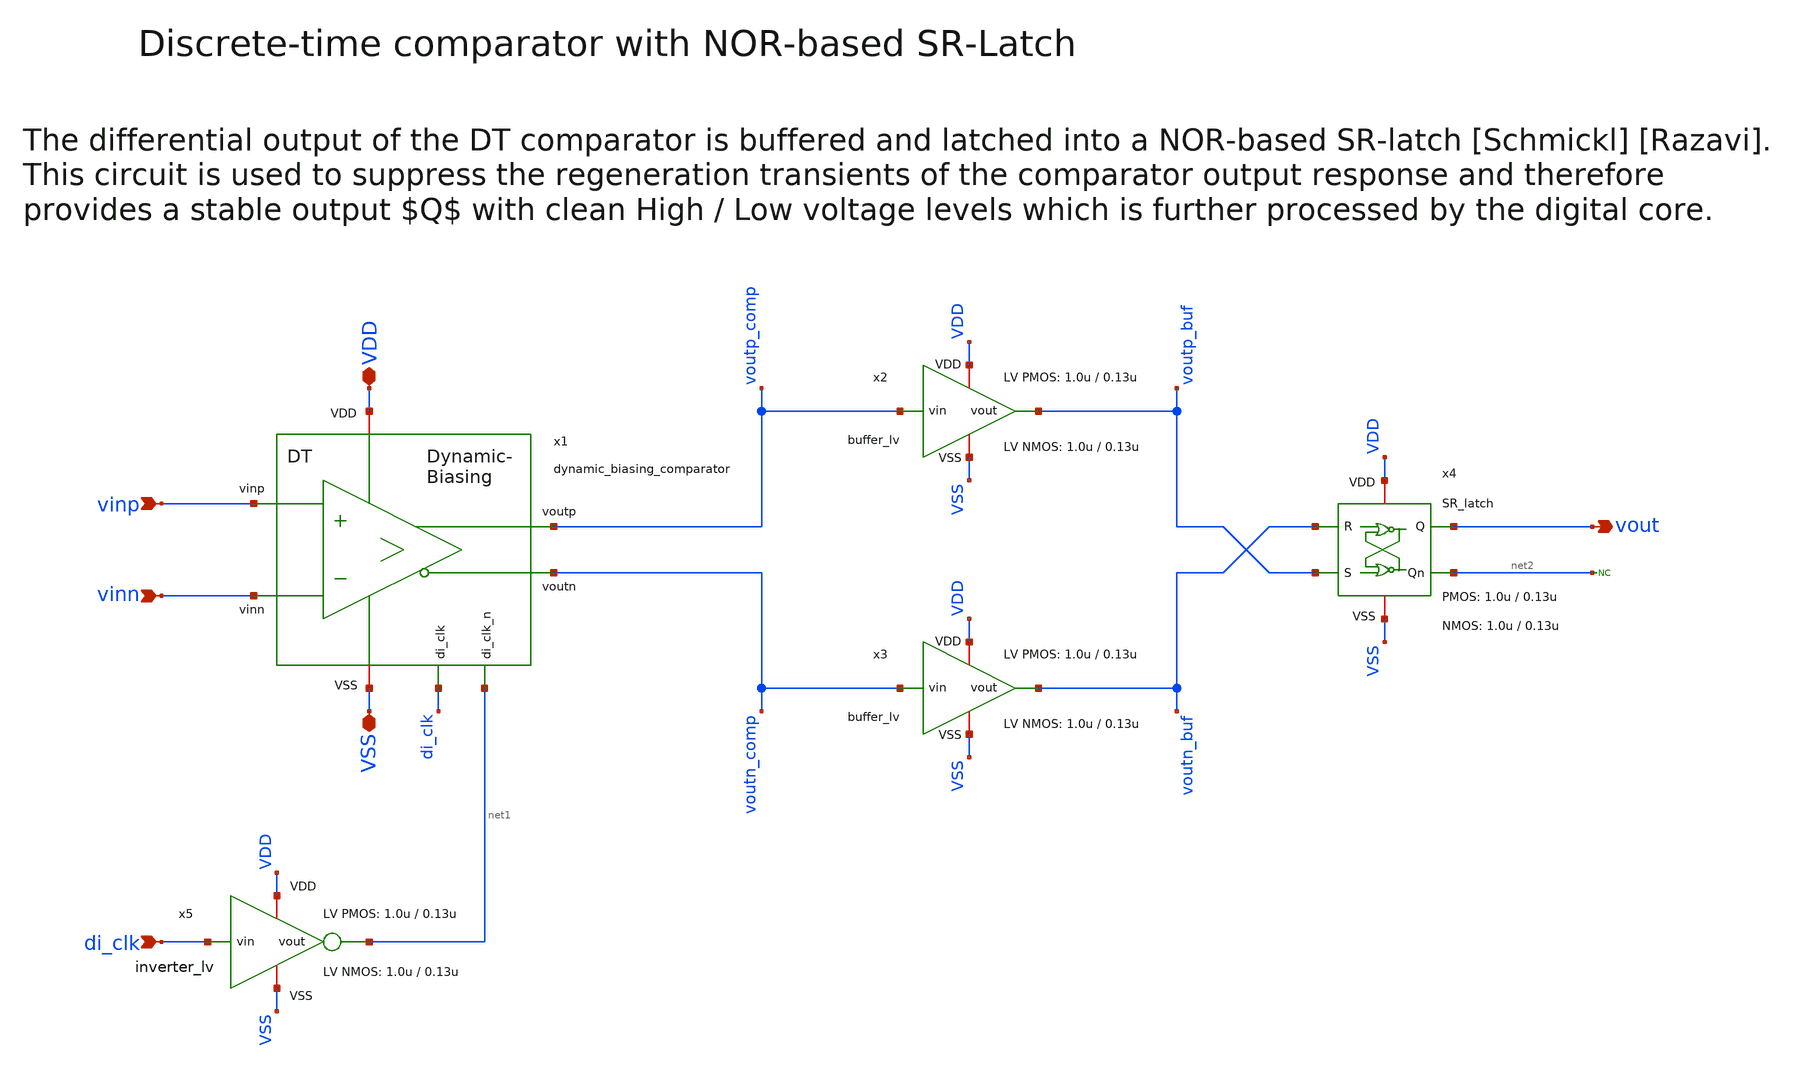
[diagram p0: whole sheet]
** sch_path: SG13G2_ATBS-ADC-main/xschem/comparator/discrete_time/DT_comparator.sch
**.subckt DT_comparator VDD vout VSS vinp vinn di_clk
*.iopin VDD
*.opin vout
*.iopin VSS
*.ipin vinp
*.ipin vinn
*.ipin di_clk
x2 VDD voutp_comp voutp_buf VSS buffer_lv W_P_INV=1.0u L_P_INV=0.13u W_N_INV=1.0u L_N_INV=0.13u
x3 VDD voutn_comp voutn_buf VSS buffer_lv W_P_INV=1.0u L_P_INV=0.13u W_N_INV=1.0u L_N_INV=0.13u
x5 VDD di_clk net1 VSS inverter_lv W_P=1.0u L_P=0.13u W_N=1.0u L_N=0.13u
* noconn #net2
x4 VDD voutp_buf net2 VSS vout voutn_buf SR_latch W_P_SR=1.0u L_P_SR=0.13u W_N_SR=1.0u L_N_SR=0.13u
x1 net1 di_clk VDD voutp_comp vinp VSS voutn_comp vinn dynamic_biasing_comparator
**.ends

* expanding   symbol:  buffer/buffer_lv.sym # of pins=4
** sym_path: SG13G2_ATBS-ADC-main/xschem/buffer/buffer_lv.sym
** sch_path: SG13G2_ATBS-ADC-main/xschem/buffer/buffer_lv.sch
.subckt buffer_lv VDD vin vout VSS  W_P_INV=3.0u L_P_INV=0.13u W_N_INV=1.0u L_N_INV=0.13u
*.ipin vin
*.iopin VDD
*.iopin VSS
*.opin vout
x1 VDD vin net1 VSS inverter_lv W_P=W_P_INV L_P=L_P_INV W_N=W_N_INV L_N=L_N_INV
x2 VDD net1 vout VSS inverter_lv W_P=W_P_INV L_P=L_P_INV W_N=W_N_INV L_N=L_N_INV
.ends


* expanding   symbol:  inverter/inverter_lv.sym # of pins=4
** sym_path: SG13G2_ATBS-ADC-main/xschem/inverter/inverter_lv.sym
** sch_path: SG13G2_ATBS-ADC-main/xschem/inverter/inverter_lv.sch
.subckt inverter_lv VDD vin vout VSS  W_P=3.0u L_P=0.13u W_N=1.0u L_N=0.13u
*.ipin vin
*.iopin VDD
*.iopin VSS
*.opin vout
XM1 vout vin VDD VDD sg13_lv_pmos w=W_P l=L_P ng=1 m=1 mm_ok=1
XM2 vout vin VSS VSS sg13_lv_nmos w=W_N l=L_N ng=1 m=1 mm_ok=1
.ends


* expanding   symbol:  comparator/SR_latch/SR_latch.sym # of pins=6
** sym_path: SG13G2_ATBS-ADC-main/xschem/comparator/SR_latch/SR_latch.sym
** sch_path: SG13G2_ATBS-ADC-main/xschem/comparator/SR_latch/SR_latch.sch
.subckt SR_latch VDD S Qn VSS Q R  W_P_SR=1.0u L_P_SR=0.13u W_N_SR=1.0u L_N_SR=0.13u
*.iopin VDD
*.opin Q
*.iopin VSS
*.ipin S
*.ipin R
*.opin Qn
x1 VDD Q R Qn VSS NOR_gate W_P=W_P_SR L_P=L_P_SR W_N=W_N_SR L_N=L_N_SR
x2 VDD Qn Q S VSS NOR_gate W_P=W_P_SR L_P=L_P_SR W_N=W_N_SR L_N=L_N_SR
.ends


* expanding   symbol:  comparator/discrete_time/Dynamic-biasing/dynamic_biasing_comparator.sym # of
*+ pins=8
** sym_path: SG13G2_ATBS-ADC-main/xschem/comparator/discrete_time/Dynamic-biasing/dynamic_biasing_comparator.sym
** sch_path: SG13G2_ATBS-ADC-main/xschem/comparator/discrete_time/Dynamic-biasing/dynamic_biasing_comparator.sch
.subckt dynamic_biasing_comparator di_clk_n di_clk VDD voutp vinp VSS voutn vinn
*.iopin VDD
*.opin voutp
*.opin voutn
*.ipin di_clk_n
*.iopin VSS
*.ipin vinp
*.ipin vinn
*.ipin di_clk
XM3a vs di_clk vctail VSS sg13_lv_nmos w=1.0u l=0.13u ng=1 m=1 mm_ok=1
XM12 voutp di_clk_n VSS VSS sg13_lv_nmos w=1.0u l=0.13u ng=1 m=1 mm_ok=1
XM8 net1 voutn VDD VDD sg13_lv_pmos w=2.0u l=0.13u ng=2 m=1 mm_ok=1
XM10 voutp voutn VSS VSS sg13_lv_nmos w=1.0u l=0.13u ng=1 m=1 mm_ok=1
XM11 voutn voutp VSS VSS sg13_lv_nmos w=1.0u l=0.13u ng=1 m=1 mm_ok=1
XM13 voutn di_clk_n VSS VSS sg13_lv_nmos w=1.0u l=0.13u ng=1 m=1 mm_ok=1
CPn vcpn VSS 300f m=1
CPp vcpp VSS 300f m=1
XM9 net2 voutp VDD VDD sg13_lv_pmos w=2.0u l=0.13u ng=2 m=1 mm_ok=1
XM6 voutp vcpn net1 VDD sg13_lv_pmos w=2.0u l=0.13u ng=2 m=1 mm_ok=1
XM7 voutn vcpp net2 VDD sg13_lv_pmos w=2.0u l=0.13u ng=2 m=1 mm_ok=1
CTAIL vctail VSS 600f m=1
XM3b vctail di_clk_n VSS VSS sg13_lv_nmos w=1.0u l=0.13u ng=1 m=1 mm_ok=1
XM1 vcpn vinp vs VSS sg13_lv_nmos w=1.0u l=0.13u ng=1 m=1 mm_ok=1
XM2 vcpp vinn vs VSS sg13_lv_nmos w=1.0u l=0.13u ng=1 m=1 mm_ok=1
XM4 vcpn di_clk VDD VDD sg13_lv_pmos w=1.0u l=0.13u ng=1 m=1 mm_ok=1
XM5 vcpp di_clk VDD VDD sg13_lv_pmos w=1.0u l=0.13u ng=1 m=1 mm_ok=1
.ends


* expanding   symbol:  comparator/NOR_gate/NOR_gate.sym # of pins=5
** sym_path: SG13G2_ATBS-ADC-main/xschem/comparator/NOR_gate/NOR_gate.sym
** sch_path: SG13G2_ATBS-ADC-main/xschem/comparator/NOR_gate/NOR_gate.sch
.subckt NOR_gate VDD C A B VSS  W_P=1.0u L_P=0.13u W_N=0.5u L_N=0.13u
*.iopin VDD
*.opin C
*.iopin VSS
*.ipin A
*.ipin B
XM1 C A VSS VSS sg13_lv_nmos w=W_N l=L_N ng=1 m=1 mm_ok=1
XM2 C B VSS VSS sg13_lv_nmos w=W_N l=L_N ng=1 m=1 mm_ok=1
XM3 C B net1 VDD sg13_lv_pmos w=W_P l=L_P ng=1 m=1 mm_ok=1
XM4 net1 A VDD VDD sg13_lv_pmos w=W_P l=L_P ng=1 m=1 mm_ok=1
XM5 C A net2 VDD sg13_lv_pmos w=W_P l=L_P ng=1 m=1 mm_ok=1
XM6 net2 B VDD VDD sg13_lv_pmos w=W_P l=L_P ng=1 m=1 mm_ok=1
.ends

.end
